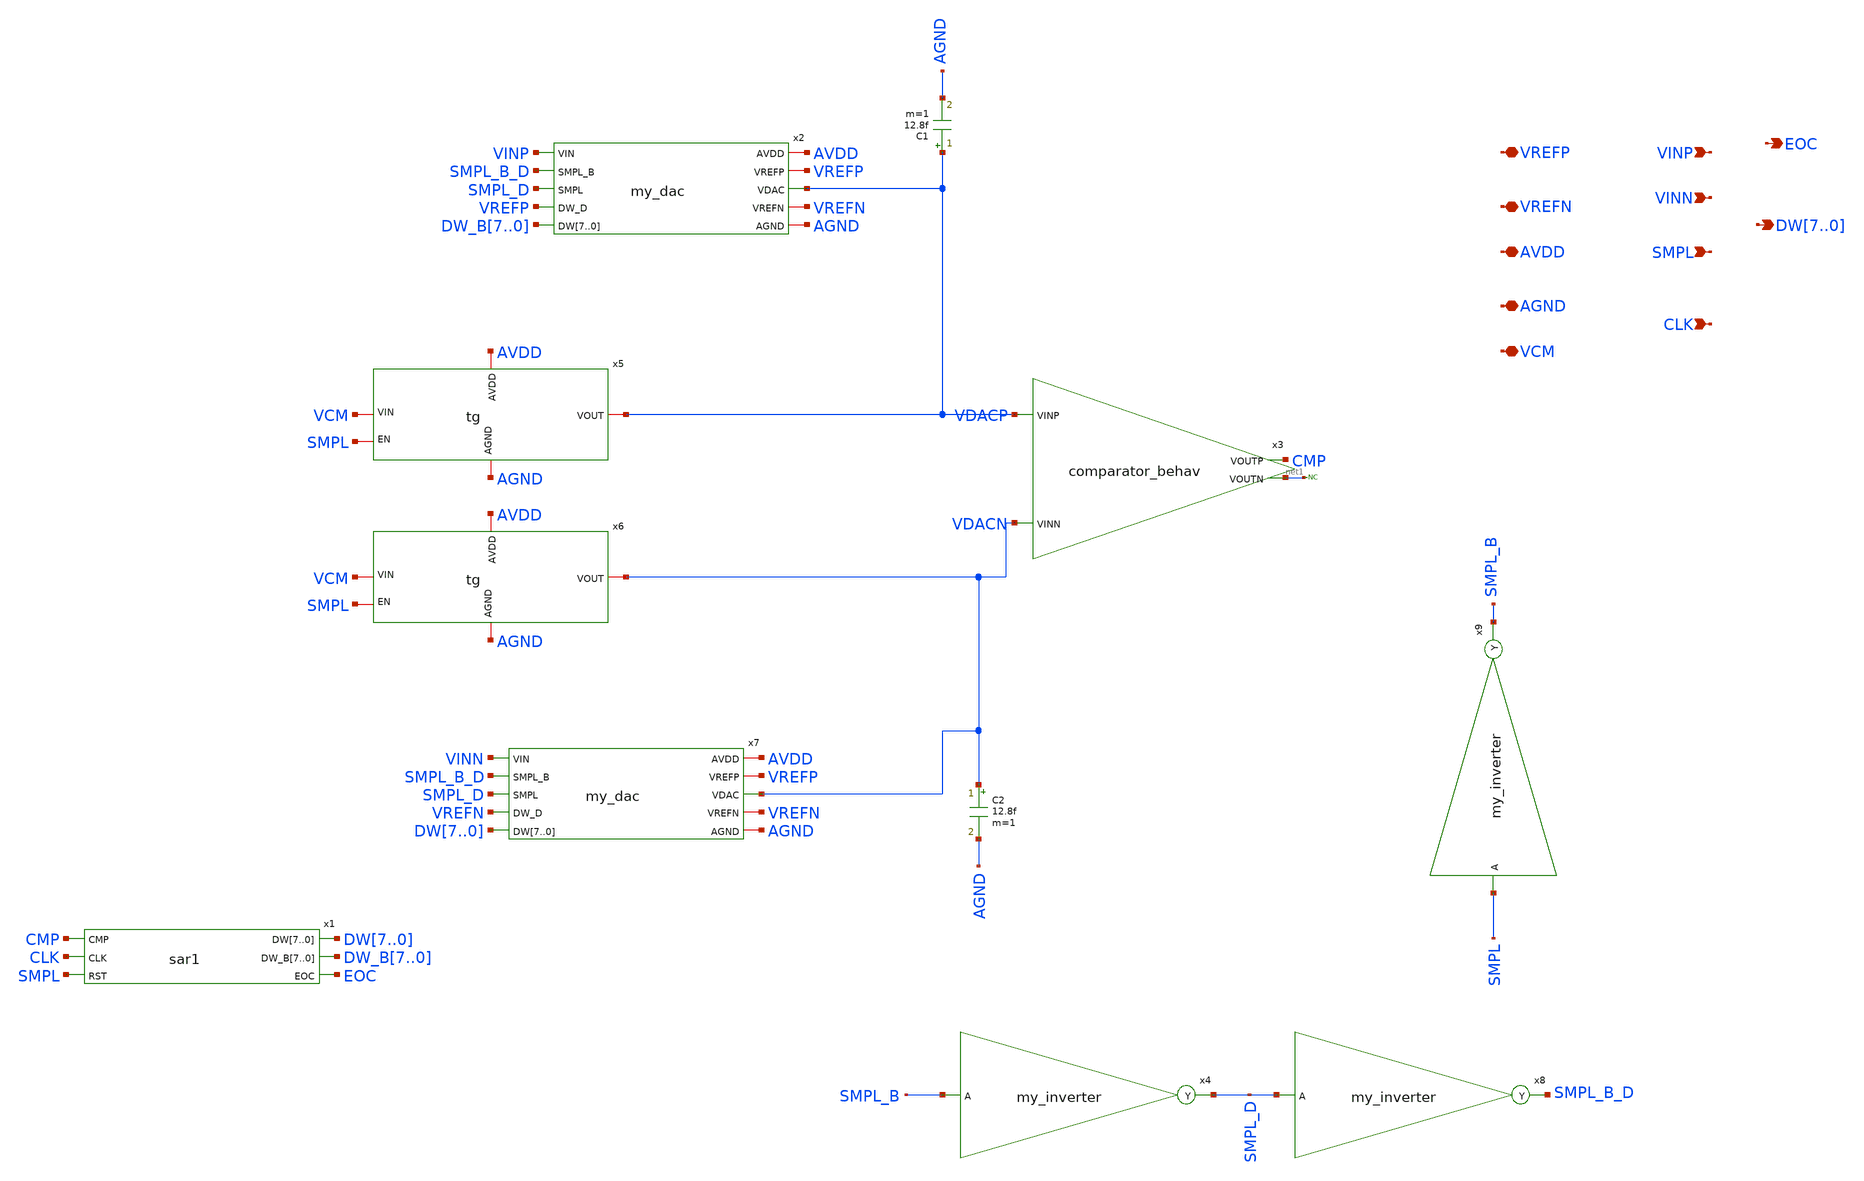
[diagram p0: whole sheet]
** sch_path: sar_adc_differential.sch
**.subckt sar_adc_differential VREFP VREFN AVDD AGND VCM VINP VINN SMPL CLK EOC
*+ DW7,DW6,DW5,DW4,DW3,DW2,DW1,DW0
*.iopin VREFP
*.iopin VREFN
*.iopin AVDD
*.iopin AGND
*.iopin VCM
*.ipin VINP
*.ipin VINN
*.ipin SMPL
*.ipin CLK
*.opin EOC
*.opin DW7,DW6,DW5,DW4,DW3,DW2,DW1,DW0
x1 CMP CLK SMPL DW7 DW6 DW5 DW4 DW3 DW2 DW1 DW0 DW_B7 DW_B6 DW_B5 DW_B4 DW_B3 DW_B2 DW_B1 DW_B0 EOC
+ sar1
x2 AVDD AGND VREFN VREFP VDACP VINP SMPL_B_D SMPL_D VREFP DW_B7 DW_B6 DW_B5 DW_B4 DW_B3 DW_B2 DW_B1
+ DW_B0 my_dac
x3 CMP VDACP VDACN net1 comparator_behav
x4 SMPL_D SMPL_B my_inverter
x5 SMPL AGND VDACP VCM AVDD tg
C1 VDACP AGND 12.8f m=1
* noconn #net1
x6 SMPL AGND VDACN VCM AVDD tg
C2 VDACN AGND 12.8f m=1
x7 AVDD AGND VREFN VREFP VDACN VINN SMPL_B_D SMPL_D VREFN DW7 DW6 DW5 DW4 DW3 DW2 DW1 DW0 my_dac
x8 SMPL_B_D SMPL_D my_inverter
x9 SMPL_B SMPL my_inverter
**.ends
.end
